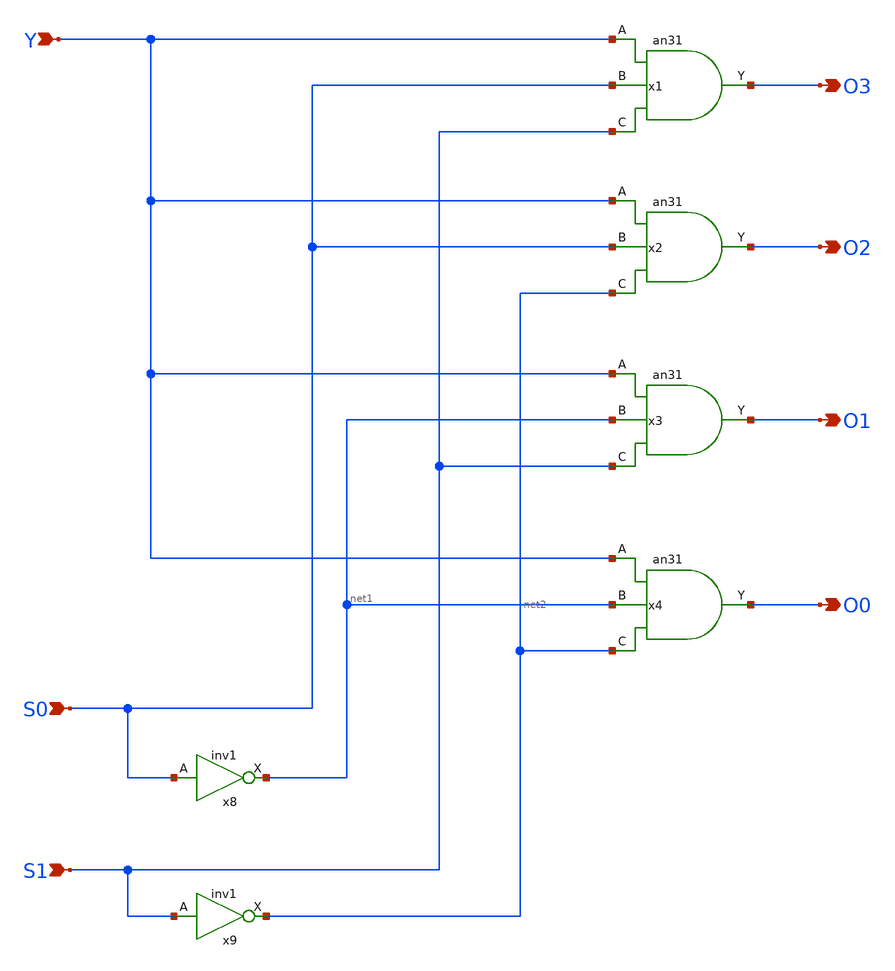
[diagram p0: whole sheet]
** sch_path: member_project/ishi-kai/4ch_demux.sch
**.subckt 4ch_demux Y S0 S1 O0 O1 O2 O3
*.ipin Y
*.ipin S0
*.ipin S1
*.opin O0
*.opin O1
*.opin O2
*.opin O3
x1 Y S0 S1 VDD GND O3 an31
x2 Y S0 net2 VDD GND O2 an31
x3 Y net1 S1 VDD GND O1 an31
x4 Y net1 net2 VDD GND O0 an31
x8 S0 VDD GND net1 inv1
x9 S1 VDD GND net2 inv1
**.ends
.end
